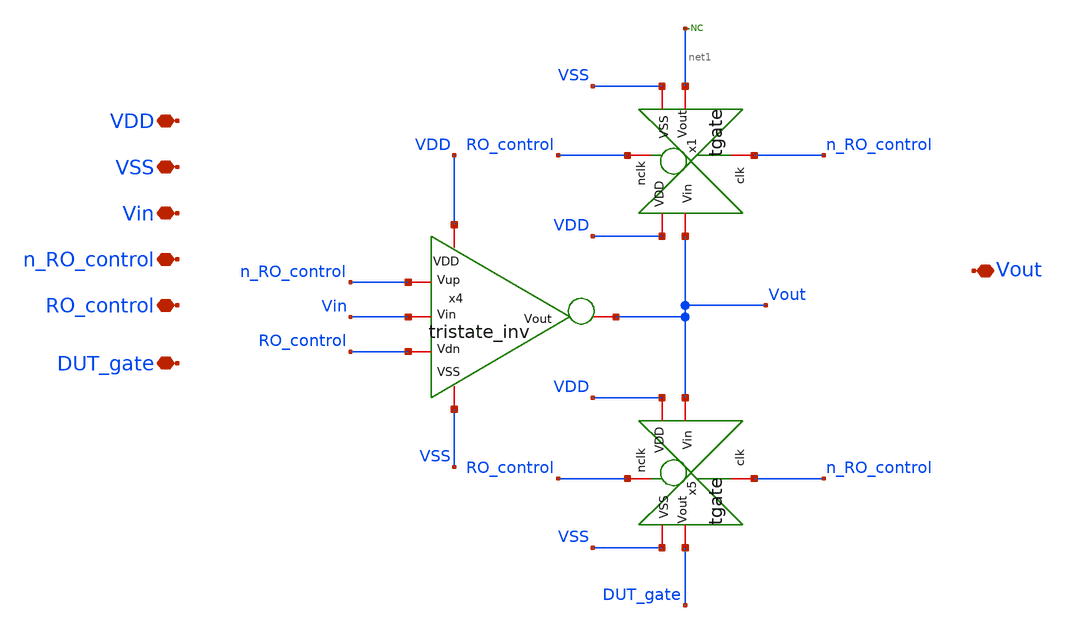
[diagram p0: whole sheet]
** sch_path: unic_cass_wrapper_user_project/ROs_reliability/rovcel3.sch
**.subckt rovcel3 VDD VSS Vin n_RO_control RO_control DUT_gate Vout
*.iopin VDD
*.iopin VSS
*.iopin Vin
*.iopin n_RO_control
*.iopin RO_control
*.iopin DUT_gate
*.iopin Vout
* noconn #net1
x4 VDD VSS Vin n_RO_control RO_control Vout tristate_inv
x1 RO_control VDD Vout net1 VSS n_RO_control tgate
x5 RO_control VDD Vout DUT_gate VSS n_RO_control tgate
**.ends

* expanding   symbol:  tristate_inv.sym # of pins=6
** sym_path: tristate_inv.sym
** sch_path: tristate_inv.sch
.subckt tristate_inv VDD VSS Vin Vup Vdn Vout
*.iopin VDD
*.iopin VSS
*.iopin Vin
*.iopin Vout
*.iopin Vup
*.iopin Vdn
XM5 Vout Vin net1 VDD sg13_lv_pmos w=3.4u l=0.45u ng=1 m=4 mm_ok=1
XM2 net2 Vin Vout VSS sg13_lv_nmos w=1.3u l=0.45u ng=1 m=4 mm_ok=1
XM1 net1 Vup VDD VDD sg13_lv_pmos w=3.4u l=0.45u ng=1 m=12 mm_ok=1
XM3 VSS Vdn net2 VSS sg13_lv_nmos w=1.3u l=0.45u ng=1 m=12 mm_ok=1
.ends


* expanding   symbol:  tgate.sym # of pins=6
** sym_path: tgate.sym
** sch_path: tgate.sch
.subckt tgate nclk VDD Vin Vout VSS clk
*.iopin nclk
*.iopin clk
*.iopin VDD
*.iopin VSS
*.iopin Vout
*.iopin Vin
XM3 Vout nclk Vin VDD sg13_lv_pmos w=3.4u l=0.45u ng=1 m=1 mm_ok=1
XM1 Vout clk Vin VSS sg13_lv_nmos w=1.3u l=0.45u ng=1 m=1 mm_ok=1
.ends

.end
